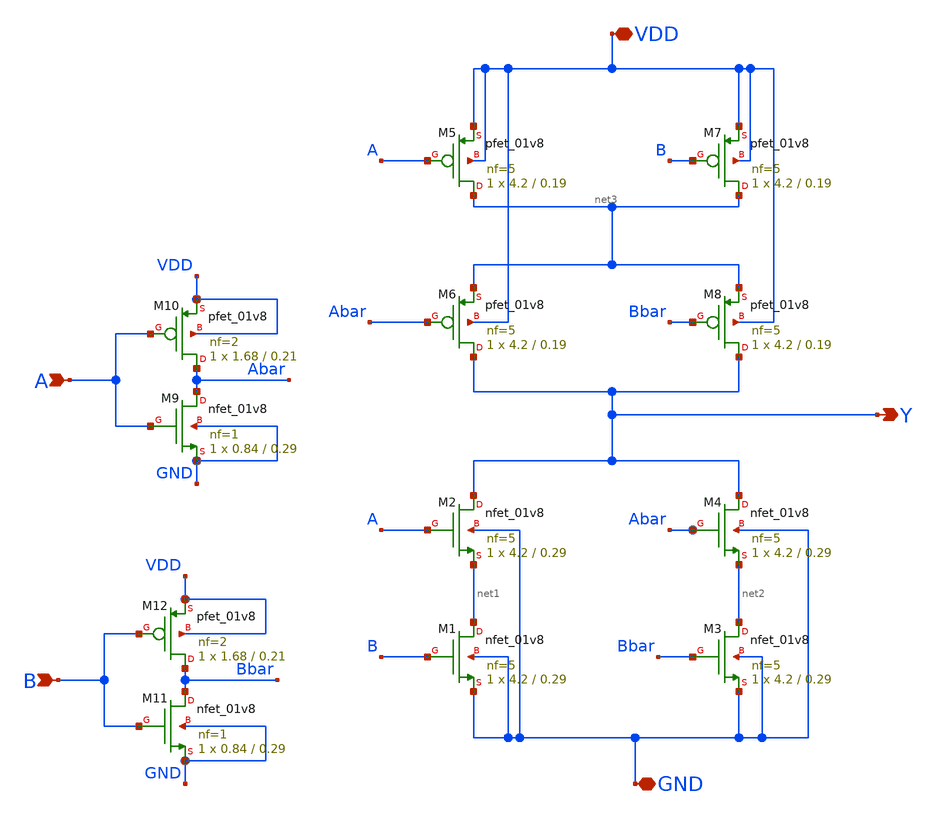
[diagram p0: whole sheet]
** sch_path: cells/XOR2X4/schematic/xor2x4.sch
**.subckt xor2x4 A Y VDD GND B
*.ipin A
*.opin Y
*.iopin VDD
*.iopin GND
*.ipin B
XM2 Y A net1 GND sky130_fd_pr__nfet_01v8 L=0.29 W=4.2 nf=5 ad='int((5 + 1)/2) * 4.2 / 5 * 0.29' as='int((5 + 2)/2) * 4.2 / 5 * 0.29'
+ pd='2*int((5 + 1)/2) * (4.2 / 5 + 0.29)' ps='2*int((5 + 2)/2) * (4.2 / 5 + 0.29)' nrd='0.29 / 4.2 ' nrs='0.29 / 4.2 '
+ sa=0 sb=0 sd=0 mult=1 m=1
XM5 net3 A VDD VDD sky130_fd_pr__pfet_01v8 L=0.19 W=4.2 nf=5 ad='int((5 + 1)/2) * 4.2 / 5 * 0.29' as='int((5 + 2)/2) * 4.2 / 5 * 0.29'
+ pd='2*int((5 + 1)/2) * (4.2 / 5 + 0.29)' ps='2*int((5 + 2)/2) * (4.2 / 5 + 0.29)' nrd='0.29 / 4.2 ' nrs='0.29 / 4.2 '
+ sa=0 sb=0 sd=0 mult=1 m=1
XM9 Abar A GND GND sky130_fd_pr__nfet_01v8 L=0.29 W=0.84 nf=1 ad='int((1 + 1)/2) * 0.84 / 1 * 0.29' as='int((1 + 2)/2) * 0.84 / 1 * 0.29'
+ pd='2*int((1 + 1)/2) * (0.84 / 1 + 0.29)' ps='2*int((1 + 2)/2) * (0.84 / 1 + 0.29)' nrd='0.29 / 0.84 '
+ nrs='0.29 / 0.84 ' sa=0 sb=0 sd=0 mult=1 m=1
XM10 Abar A VDD VDD sky130_fd_pr__pfet_01v8 L=0.21 W=1.68 nf=2 ad='int((2 + 1)/2) * 1.68 / 2 * 0.29'
+ as='int((2 + 2)/2) * 1.68 / 2 * 0.29' pd='2*int((2 + 1)/2) * (1.68 / 2 + 0.29)' ps='2*int((2 + 2)/2) * (1.68 / 2 + 0.29)'
+ nrd='0.29 / 1.68 ' nrs='0.29 / 1.68 ' sa=0 sb=0 sd=0 mult=1 m=1
XM6 Y Abar net3 VDD sky130_fd_pr__pfet_01v8 L=0.19 W=4.2 nf=5 ad='int((5 + 1)/2) * 4.2 / 5 * 0.29' as='int((5 + 2)/2) * 4.2 / 5 * 0.29'
+ pd='2*int((5 + 1)/2) * (4.2 / 5 + 0.29)' ps='2*int((5 + 2)/2) * (4.2 / 5 + 0.29)' nrd='0.29 / 4.2 ' nrs='0.29 / 4.2 '
+ sa=0 sb=0 sd=0 mult=1 m=1
XM8 Y Bbar net3 VDD sky130_fd_pr__pfet_01v8 L=0.19 W=4.2 nf=5 ad='int((5 + 1)/2) * 4.2 / 5 * 0.29' as='int((5 + 2)/2) * 4.2 / 5 * 0.29'
+ pd='2*int((5 + 1)/2) * (4.2 / 5 + 0.29)' ps='2*int((5 + 2)/2) * (4.2 / 5 + 0.29)' nrd='0.29 / 4.2 ' nrs='0.29 / 4.2 '
+ sa=0 sb=0 sd=0 mult=1 m=1
XM7 net3 B VDD VDD sky130_fd_pr__pfet_01v8 L=0.19 W=4.2 nf=5 ad='int((5 + 1)/2) * 4.2 / 5 * 0.29' as='int((5 + 2)/2) * 4.2 / 5 * 0.29'
+ pd='2*int((5 + 1)/2) * (4.2 / 5 + 0.29)' ps='2*int((5 + 2)/2) * (4.2 / 5 + 0.29)' nrd='0.29 / 4.2 ' nrs='0.29 / 4.2 '
+ sa=0 sb=0 sd=0 mult=1 m=1
XM1 net1 B GND GND sky130_fd_pr__nfet_01v8 L=0.29 W=4.2 nf=5 ad='int((5 + 1)/2) * 4.2 / 5 * 0.29' as='int((5 + 2)/2) * 4.2 / 5 * 0.29'
+ pd='2*int((5 + 1)/2) * (4.2 / 5 + 0.29)' ps='2*int((5 + 2)/2) * (4.2 / 5 + 0.29)' nrd='0.29 / 4.2 ' nrs='0.29 / 4.2 '
+ sa=0 sb=0 sd=0 mult=1 m=1
XM4 Y Abar net2 GND sky130_fd_pr__nfet_01v8 L=0.29 W=4.2 nf=5 ad='int((5 + 1)/2) * 4.2 / 5 * 0.29' as='int((5 + 2)/2) * 4.2 / 5 * 0.29'
+ pd='2*int((5 + 1)/2) * (4.2 / 5 + 0.29)' ps='2*int((5 + 2)/2) * (4.2 / 5 + 0.29)' nrd='0.29 / 4.2 ' nrs='0.29 / 4.2 '
+ sa=0 sb=0 sd=0 mult=1 m=1
XM3 net2 Bbar GND GND sky130_fd_pr__nfet_01v8 L=0.29 W=4.2 nf=5 ad='int((5 + 1)/2) * 4.2 / 5 * 0.29'
+ as='int((5 + 2)/2) * 4.2 / 5 * 0.29' pd='2*int((5 + 1)/2) * (4.2 / 5 + 0.29)' ps='2*int((5 + 2)/2) * (4.2 / 5 + 0.29)'
+ nrd='0.29 / 4.2 ' nrs='0.29 / 4.2 ' sa=0 sb=0 sd=0 mult=1 m=1
XM12 Bbar B VDD VDD sky130_fd_pr__pfet_01v8 L=0.21 W=1.68 nf=2 ad='int((2 + 1)/2) * 1.68 / 2 * 0.29'
+ as='int((2 + 2)/2) * 1.68 / 2 * 0.29' pd='2*int((2 + 1)/2) * (1.68 / 2 + 0.29)' ps='2*int((2 + 2)/2) * (1.68 / 2 + 0.29)'
+ nrd='0.29 / 1.68 ' nrs='0.29 / 1.68 ' sa=0 sb=0 sd=0 mult=1 m=1
XM11 Bbar B GND GND sky130_fd_pr__nfet_01v8 L=0.29 W=0.84 nf=1 ad='int((1 + 1)/2) * 0.84 / 1 * 0.29'
+ as='int((1 + 2)/2) * 0.84 / 1 * 0.29' pd='2*int((1 + 1)/2) * (0.84 / 1 + 0.29)' ps='2*int((1 + 2)/2) * (0.84 / 1 + 0.29)'
+ nrd='0.29 / 0.84 ' nrs='0.29 / 0.84 ' sa=0 sb=0 sd=0 mult=1 m=1
**.ends
.end
